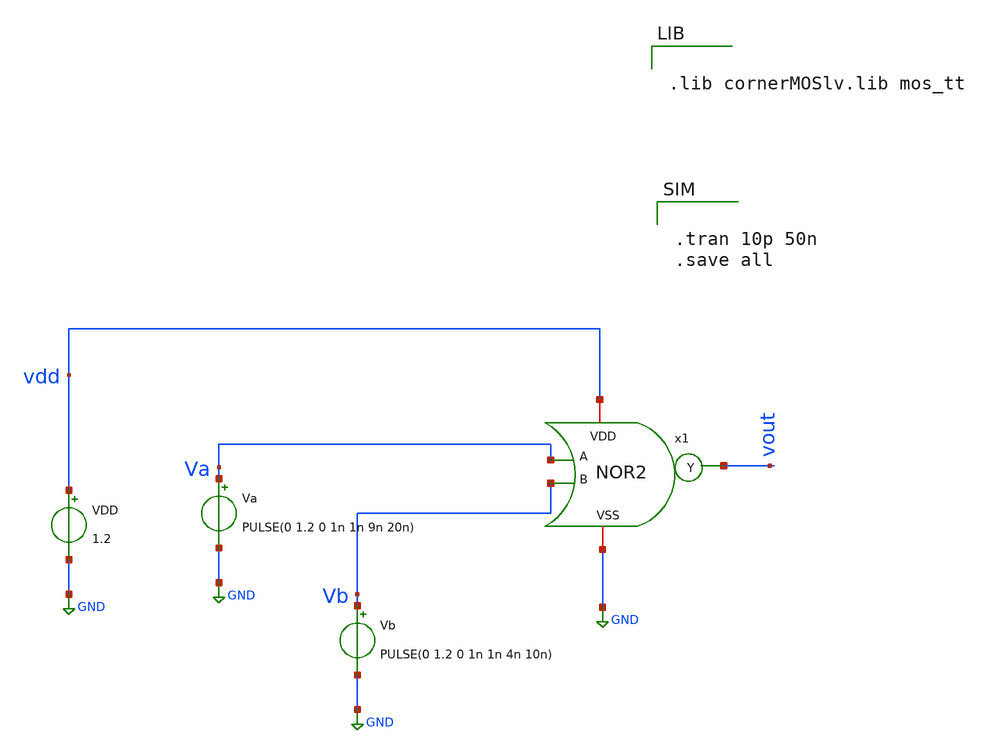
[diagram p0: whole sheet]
** sch_path: TestNAND.sch
**.subckt TestNAND
Va Va GND PULSE(0 1.2 0 1n 1n 9n 20n)
VDD vdd GND 1.2
Vb Vb GND PULSE(0 1.2 0 1n 1n 4n 10n)
x1 vdd Va vout Vb GND NOR2
**** begin user architecture code


.lib cornerMOSlv.lib mos_tt




.tran 10p 50n
.save all


**** end user architecture code
**.ends

* expanding   symbol:  /foss/designs/LogicGate/NOR2.sym # of pins=5
** sym_path: LogicGate/NOR2.sym
** sch_path: LogicGate/NOR2.sch
.subckt NOR2 VDD A Y B VSS
*.ipin A
*.ipin B
*.opin Y
*.iopin VDD
*.iopin VSS
XXM1 net1 A VDD VDD sg13_lv_pmos w=0.15u l=0.13u ng=1 m=1 mm_ok=1
XXM2 Y B net1 VDD sg13_lv_pmos w=0.15u l=0.13u ng=1 m=1 mm_ok=1
XXM3 Y A VSS VSS sg13_lv_nmos w=0.15u l=0.13u ng=1 m=1 mm_ok=1
XXM4 Y B VSS VSS sg13_lv_nmos w=0.15u l=0.13u ng=1 m=1 mm_ok=1
.ends

.GLOBAL GND
.end
